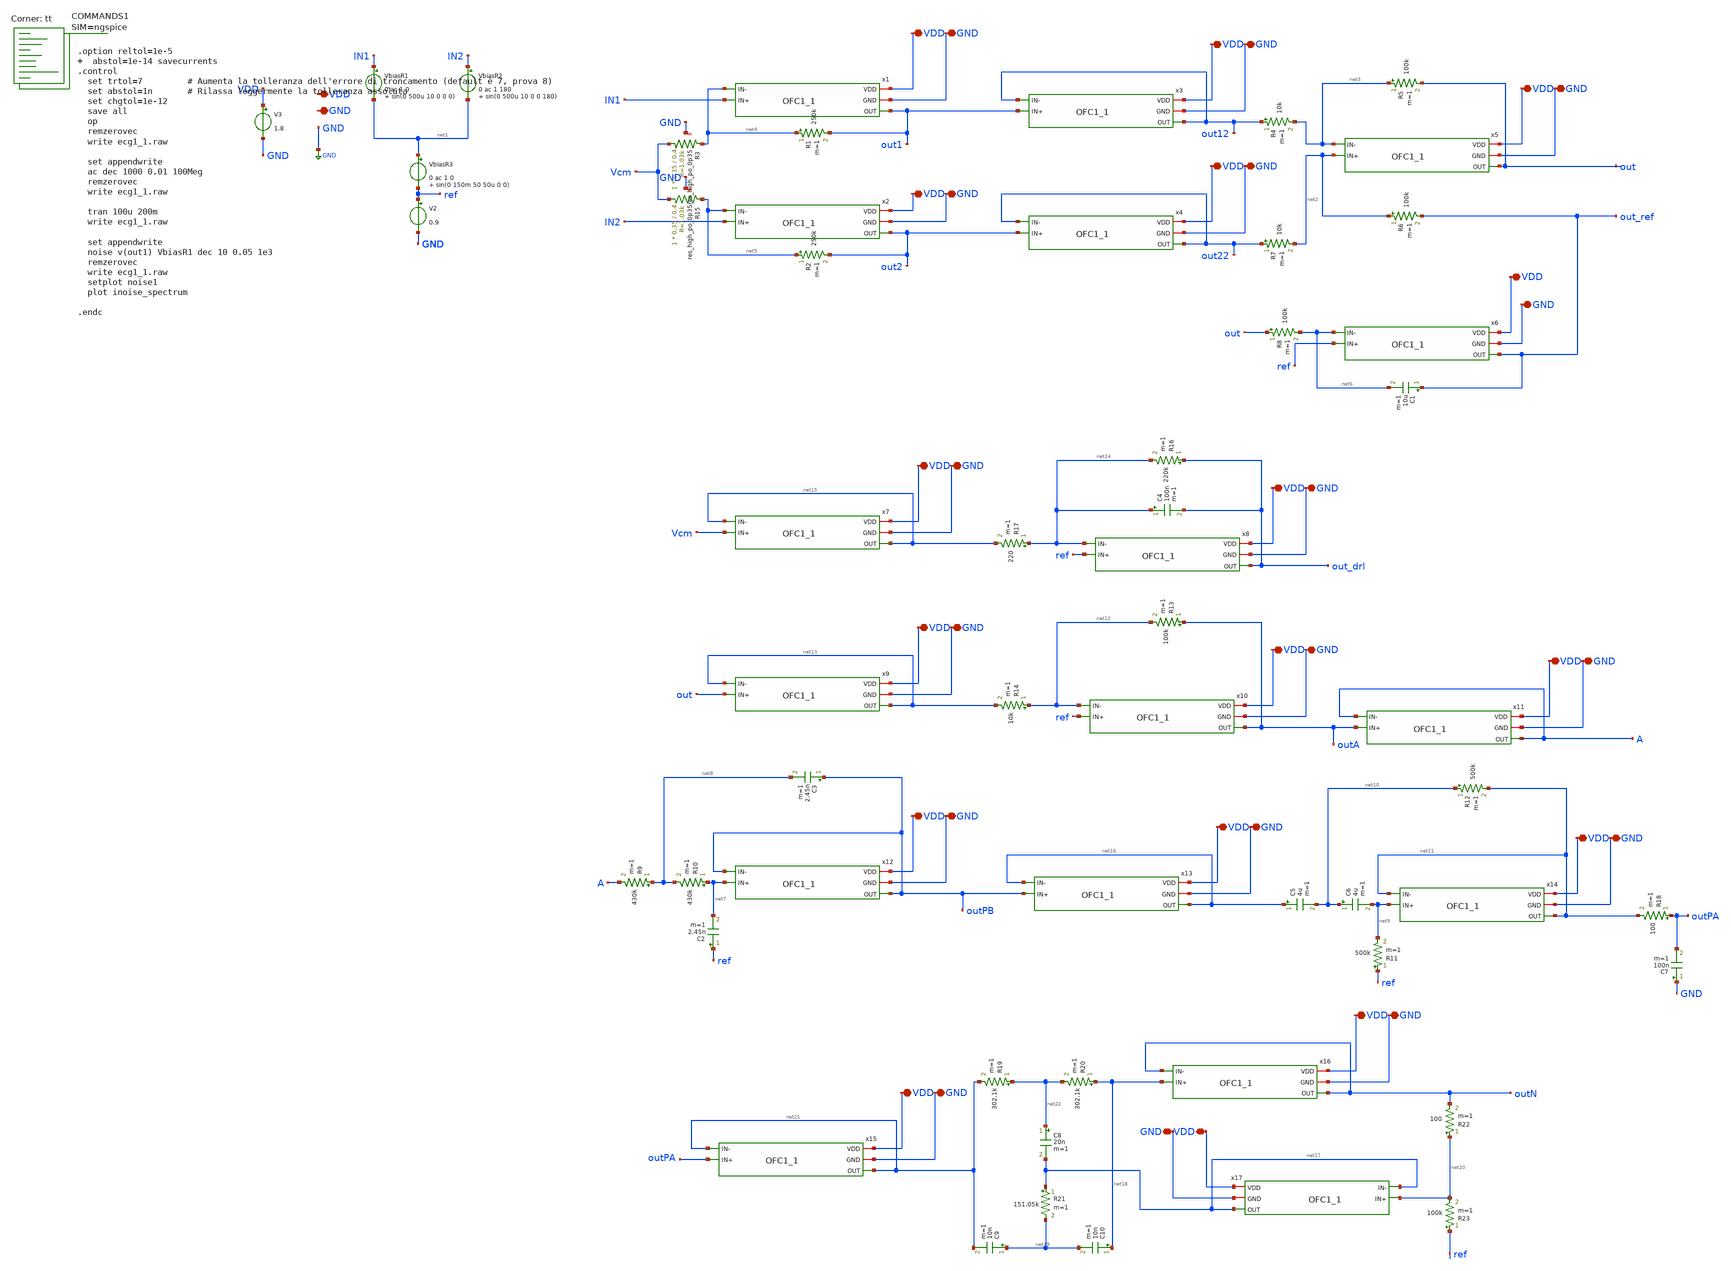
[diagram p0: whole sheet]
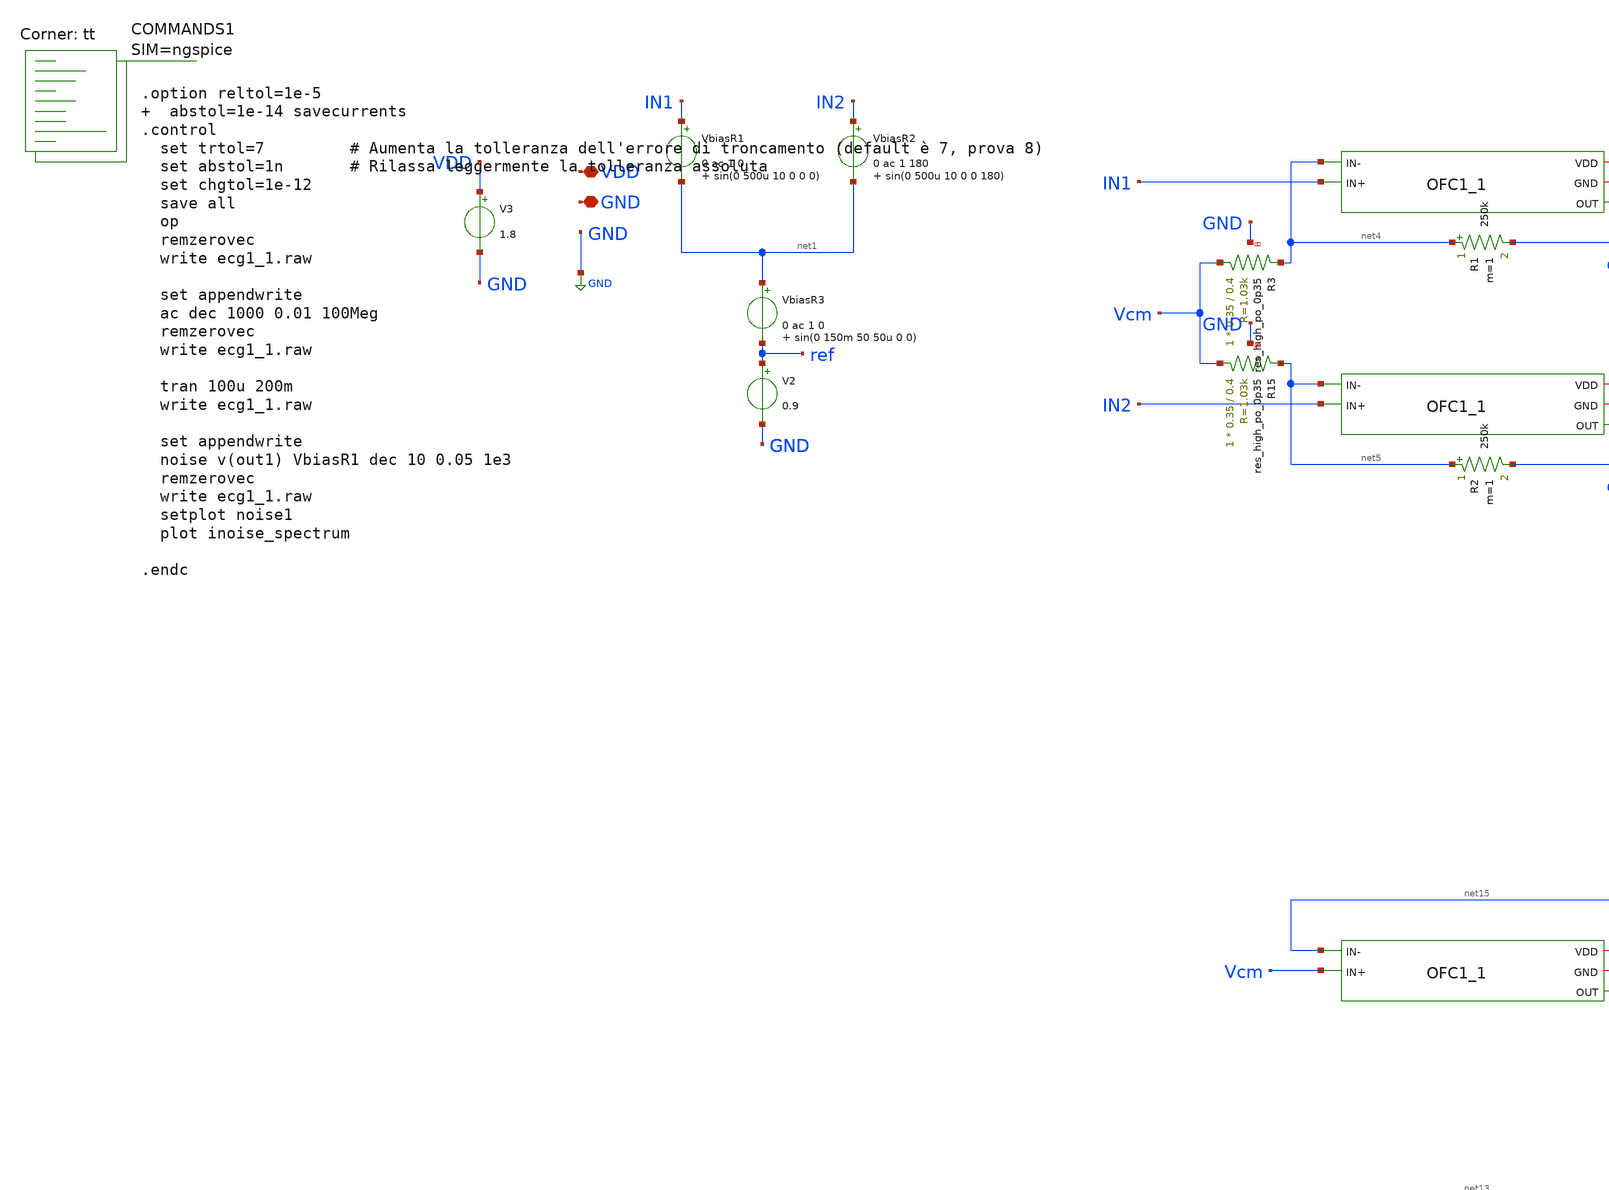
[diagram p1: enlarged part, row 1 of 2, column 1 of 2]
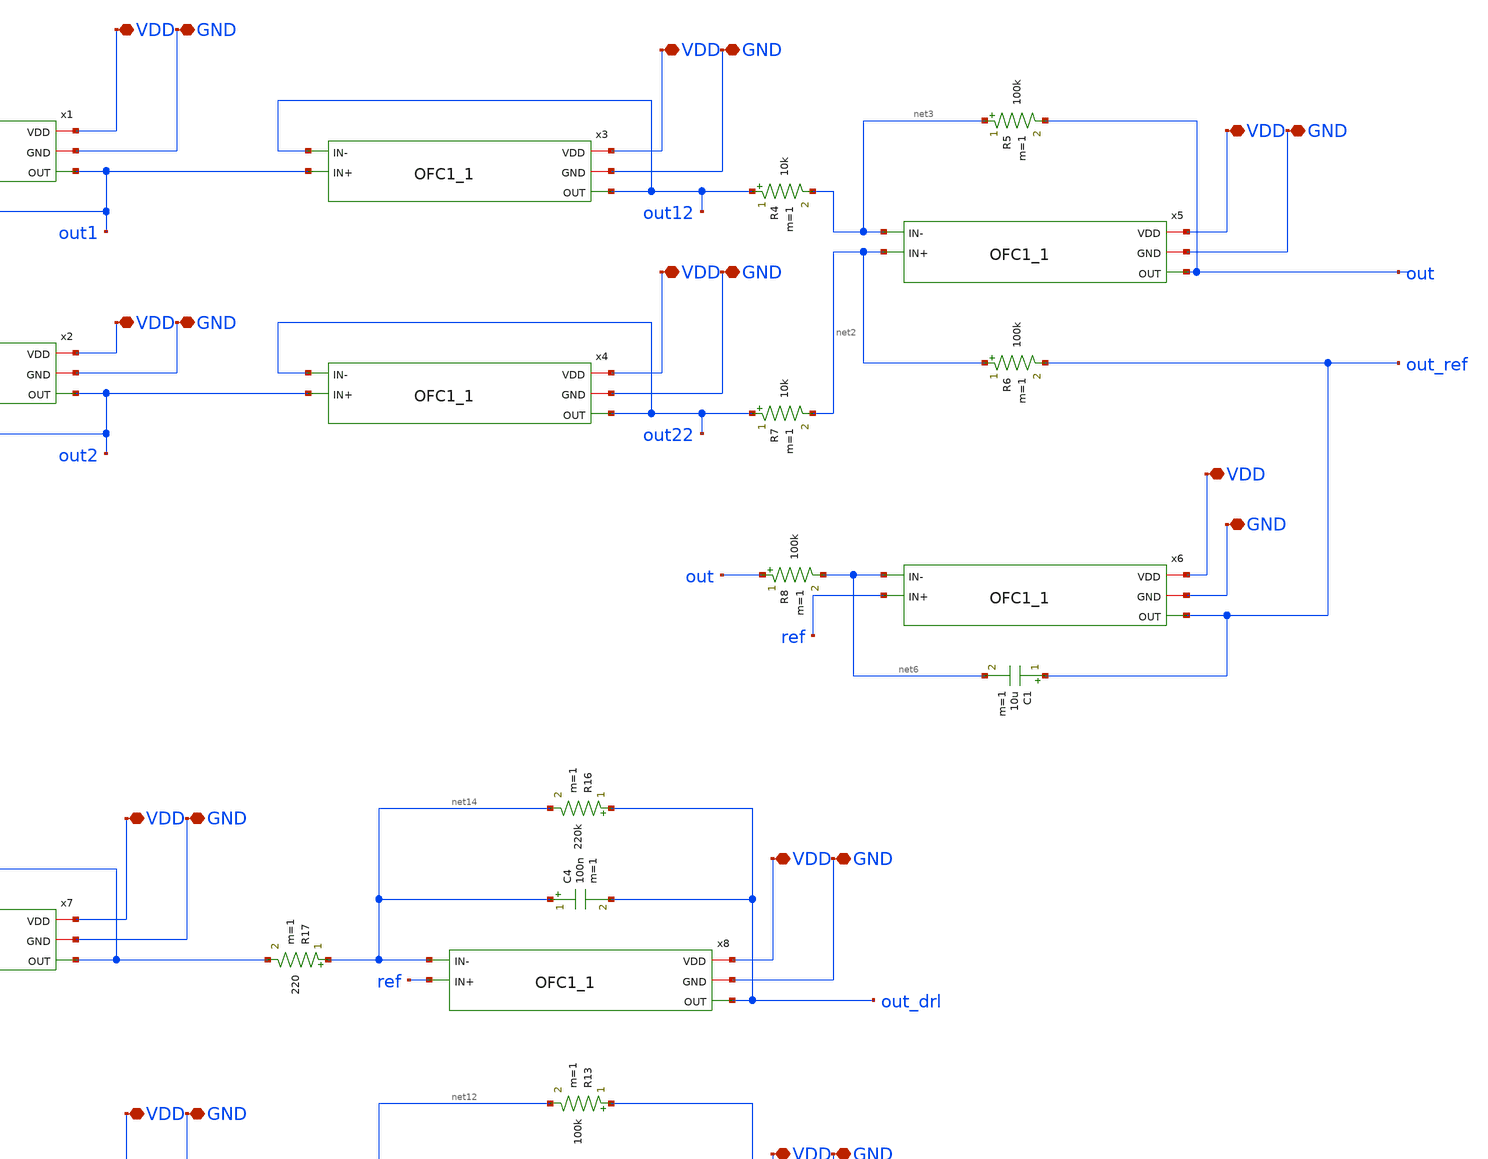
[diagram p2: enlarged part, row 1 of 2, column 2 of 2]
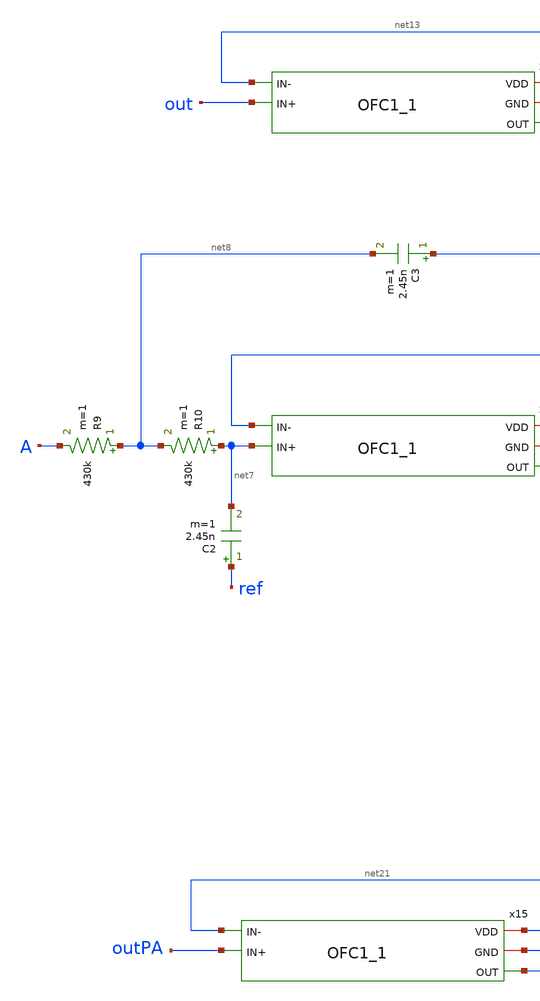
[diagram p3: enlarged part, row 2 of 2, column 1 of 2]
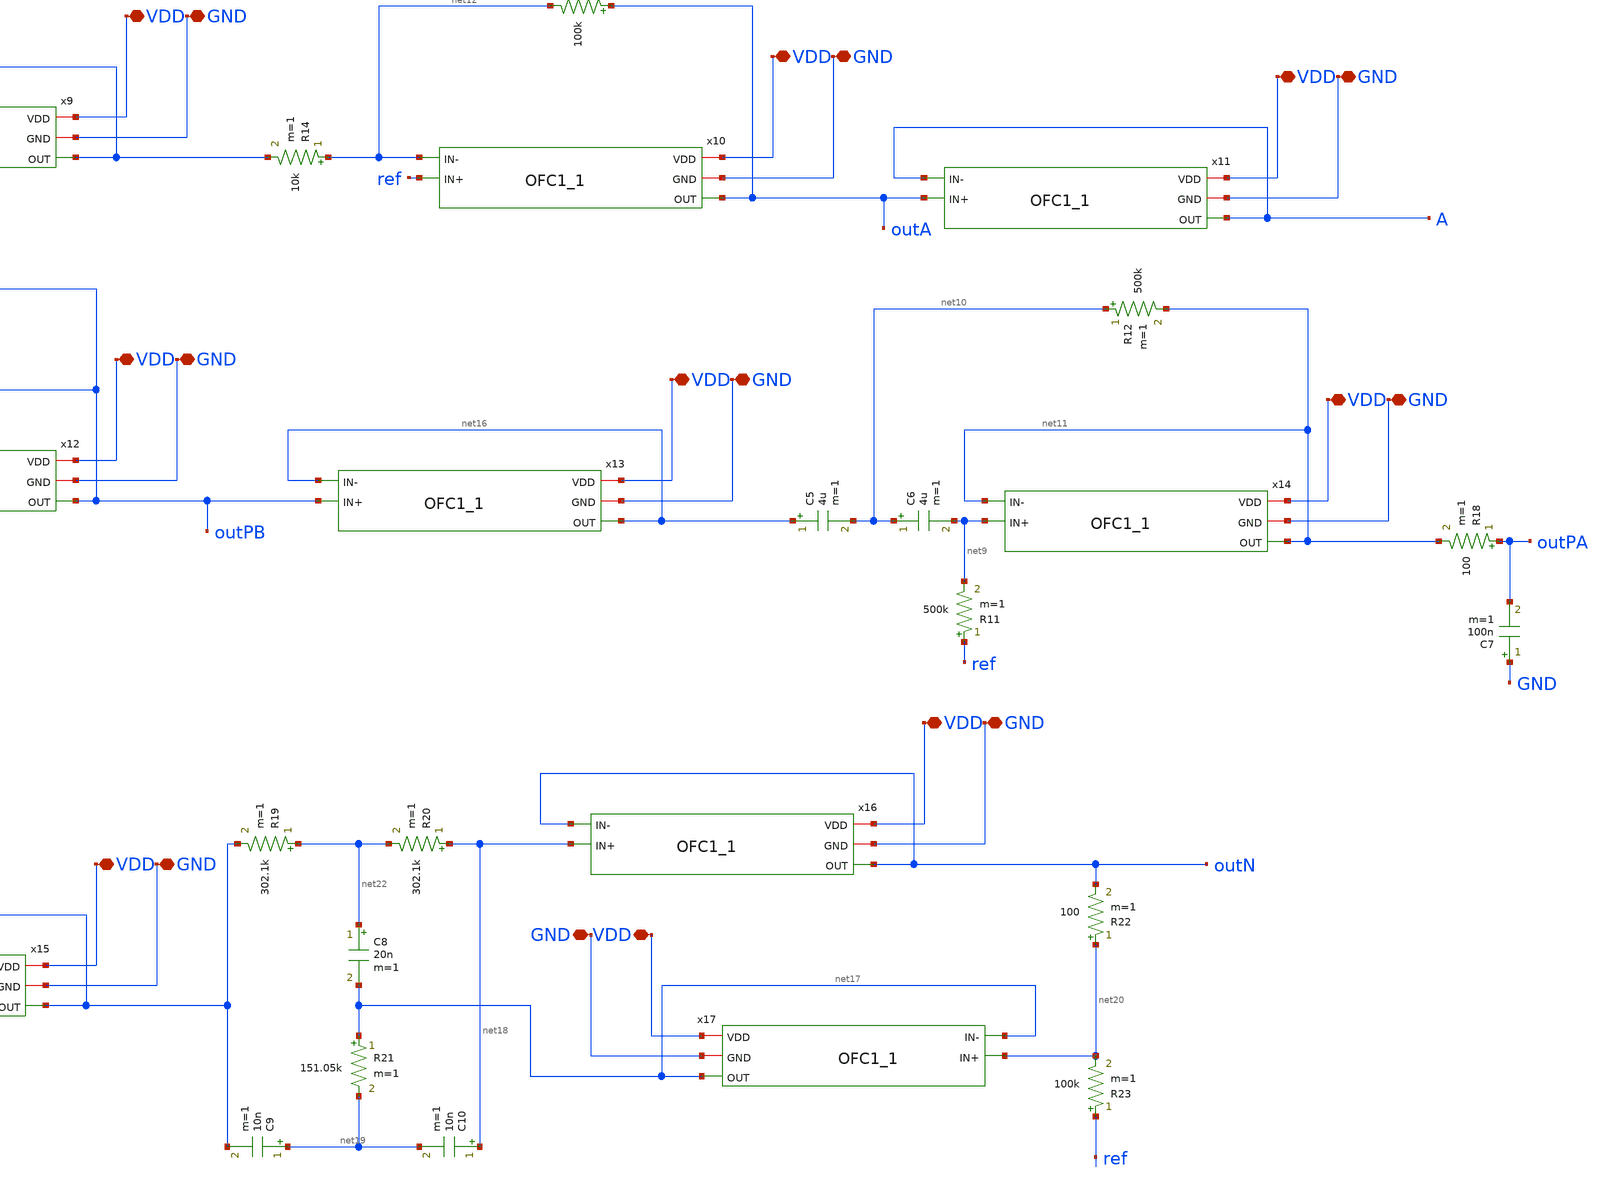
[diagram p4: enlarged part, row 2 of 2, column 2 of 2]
** sch_path: xschem/ecg1_1.sch
**.subckt ecg1_1 VDD GND VDD VDD GND GND VDD GND VDD GND VDD GND VDD GND VDD GND VDD GND VDD GND VDD
*+ GND VDD GND VDD GND VDD GND VDD GND VDD GND VDD GND VDD GND
*.iopin VDD
*.iopin GND
*.iopin VDD
*.iopin VDD
*.iopin GND
*.iopin GND
*.iopin VDD
*.iopin GND
*.iopin VDD
*.iopin GND
*.iopin VDD
*.iopin GND
*.iopin VDD
*.iopin GND
*.iopin VDD
*.iopin GND
*.iopin VDD
*.iopin GND
*.iopin VDD
*.iopin GND
*.iopin VDD
*.iopin GND
*.iopin VDD
*.iopin GND
*.iopin VDD
*.iopin GND
*.iopin VDD
*.iopin GND
*.iopin VDD
*.iopin GND
*.iopin VDD
*.iopin GND
*.iopin VDD
*.iopin GND
*.iopin VDD
*.iopin GND
V3 VDD GND 1.8
VbiasR1 IN1 net1 0 ac 1 0 sin(0 500u 10 0 0 0)
V2 ref GND 0.9
VbiasR2 IN2 net1 0 ac 1 180 sin(0 500u 10 0 0 180)
R1 net4 out1 250k m=1
R2 net5 out2 250k m=1
R6 net2 out_ref 100k m=1
R8 out net6 100k m=1
C1 out_ref net6 10u m=1
R5 net3 out 100k m=1
R4 out12 net3 10k m=1
R7 out22 net2 10k m=1
R9 net8 A 430k m=1
C2 ref net7 2.45n m=1
R10 net7 net8 430k m=1
C3 outPB net8 2.45n m=1
R11 ref net9 500k m=1
C5 net16 net10 4u m=1
C6 net10 net9 4u m=1
R13 outA net12 100k m=1
R14 net12 net13 10k m=1
R16 out_drl net14 220k m=1
R17 net14 net15 220 m=1
C4 net14 out_drl 100n m=1
C7 GND outPA 100n m=1
R18 outPA net11 100 m=1
R12 net10 net11 500k m=1
XR3 Vcm net4 GND sky130_fd_pr__res_high_po_0p35 L=0.4 mult=1 m=1
XR15 Vcm net5 GND sky130_fd_pr__res_high_po_0p35 L=0.4 mult=1 m=1
R19 net22 net21 302.1k m=1
R20 net18 net22 302.1k m=1
R21 net17 net19 151.05k m=1
C8 net22 net17 20n m=1
C9 net19 net21 10n m=1
C10 net18 net19 10n m=1
R22 net20 outN 100 m=1
R23 ref net20 100k m=1
x1 VDD GND out1 net4 IN1 OFC1_1
x2 VDD GND out2 net5 IN2 OFC1_1
x3 VDD GND out12 out12 out1 OFC1_1
x4 VDD GND out22 out22 out2 OFC1_1
x5 VDD GND out net3 net2 OFC1_1
x6 VDD GND out_ref net6 ref OFC1_1
x7 VDD GND net15 net15 Vcm OFC1_1
x8 VDD GND out_drl net14 ref OFC1_1
x9 VDD GND net13 net13 out OFC1_1
x10 VDD GND outA net12 ref OFC1_1
x11 VDD GND A A outA OFC1_1
x12 VDD GND outPB outPB net7 OFC1_1
x13 VDD GND net16 net16 outPB OFC1_1
x14 VDD GND net11 net11 net9 OFC1_1
x15 VDD GND net21 net21 outPA OFC1_1
x16 VDD GND outN outN net18 OFC1_1
x17 VDD GND net17 net17 net20 OFC1_1
VbiasR3 net1 ref 0 ac 1 0 sin(0 150m 50 50u 0 0)
**** begin user architecture code



.option reltol=1e-5   abstol=1e-14 savecurrents
.control
  set trtol=7         # Aumenta la tolleranza dell'errore di troncamento (default è 7, prova 8)
  set abstol=1n       # Rilassa leggermente la tolleranza assoluta
  set chgtol=1e-12
  save all
  op
  remzerovec
  write ecg1_1.raw

  set appendwrite
  ac dec 1000 0.01 100Meg
  remzerovec
  write ecg1_1.raw

  tran 100u 200m
  write ecg1_1.raw

  set appendwrite
  noise v(out1) VbiasR1 dec 10 0.05 1e3
  remzerovec
  write ecg1_1.raw
  setplot noise1
  plot inoise_spectrum

.endc



.lib $::SKYWATER_MODELS/sky130.lib.spice tt
**** end user architecture code
**.ends

* expanding   symbol:  OFC1_1.sym # of pins=5
** sym_path: xschem/OFC1_1.sym
** sch_path: xschem/OFC1_1.sch
.subckt OFC1_1 VDD GND OUT IN- IN+
*.iopin VDD
*.iopin GND
*.ipin IN+
*.ipin IN-
*.opin OUT
XR2 Vb VDD GND sky130_fd_pr__res_xhigh_po_0p35 L=5 mult=1 m=1
XR3 GND Vb GND sky130_fd_pr__res_xhigh_po_0p35 L=13.2 mult=1 m=1
XR1 Vc VDD GND sky130_fd_pr__res_xhigh_po_0p35 L=5 mult=1 m=1
XR4 GND Vc GND sky130_fd_pr__res_xhigh_po_0p35 L=3.07 mult=1 m=1
XR5 Vc1 VDD GND sky130_fd_pr__res_xhigh_po_0p35 L=5 mult=1 m=1
XR6 GND Vc1 GND sky130_fd_pr__res_xhigh_po_0p35 L=13.2 mult=1 m=1
XR7 Vc2 VDD GND sky130_fd_pr__res_xhigh_po_0p35 L=5 mult=1 m=1
XR8 GND Vc2 GND sky130_fd_pr__res_xhigh_po_0p35 L=1.4 mult=1 m=1
XM11 S Vb VDD VDD sky130_fd_pr__pfet_01v8_lvt L=1 W=45 nf=3 ad='int((nf+1)/2) * W/nf * 0.29' as='int((nf+2)/2)
+ * W/nf * 0.29' pd='2*int((nf+1)/2) * (W/nf + 0.29)' ps='2*int((nf+2)/2) * (W/nf + 0.29)' nrd='0.29 /
+ W' nrs='0.29 / W' sa=0 sb=0 sd=0 mult=10 m=10
XM1 D1 IN+ S S sky130_fd_pr__pfet_01v8_lvt L=10 W=50 nf=2 ad='int((nf+1)/2) * W/nf * 0.29' as='int((nf+2)/2)
+ * W/nf * 0.29' pd='2*int((nf+1)/2) * (W/nf + 0.29)' ps='2*int((nf+2)/2) * (W/nf + 0.29)' nrd='0.29 /
+ W' nrs='0.29 / W' sa=0 sb=0 sd=0 mult=2 m=2
XM2 D2 IN- S S sky130_fd_pr__pfet_01v8_lvt L=10 W=50 nf=2 ad='int((nf+1)/2) * W/nf * 0.29' as='int((nf+2)/2)
+ * W/nf * 0.29' pd='2*int((nf+1)/2) * (W/nf + 0.29)' ps='2*int((nf+2)/2) * (W/nf + 0.29)' nrd='0.29 /
+ W' nrs='0.29 / W' sa=0 sb=0 sd=0 mult=2 m=2
XM3 OUT Vc1 D2 GND sky130_fd_pr__nfet_01v8_lvt L=1 W=4 nf=1 ad='int((nf+1)/2) * W/nf * 0.29' as='int((nf+2)/2)
+ * W/nf * 0.29' pd='2*int((nf+1)/2) * (W/nf + 0.29)' ps='2*int((nf+2)/2) * (W/nf + 0.29)' nrd='0.29 /
+ W' nrs='0.29 / W' sa=0 sb=0 sd=0 mult=1 m=1
XM4 D2 Vc GND GND sky130_fd_pr__nfet_01v8_lvt L=1 W=8 nf=1 ad='int((nf+1)/2) * W/nf * 0.29' as='int((nf+2)/2)
+ * W/nf * 0.29' pd='2*int((nf+1)/2) * (W/nf + 0.29)' ps='2*int((nf+2)/2) * (W/nf + 0.29)' nrd='0.29 /
+ W' nrs='0.29 / W' sa=0 sb=0 sd=0 mult=1 m=1
XM5 D1 Vc GND GND sky130_fd_pr__nfet_01v8_lvt L=1 W=8 nf=1 ad='int((nf+1)/2) * W/nf * 0.29' as='int((nf+2)/2)
+ * W/nf * 0.29' pd='2*int((nf+1)/2) * (W/nf + 0.29)' ps='2*int((nf+2)/2) * (W/nf + 0.29)' nrd='0.29 /
+ W' nrs='0.29 / W' sa=0 sb=0 sd=0 mult=1 m=1
XM6 G Vc1 D1 GND sky130_fd_pr__nfet_01v8_lvt L=1 W=4 nf=1 ad='int((nf+1)/2) * W/nf * 0.29' as='int((nf+2)/2)
+ * W/nf * 0.29' pd='2*int((nf+1)/2) * (W/nf + 0.29)' ps='2*int((nf+2)/2) * (W/nf + 0.29)' nrd='0.29 /
+ W' nrs='0.29 / W' sa=0 sb=0 sd=0 mult=1 m=1
XM7 G Vc2 D9 VDD sky130_fd_pr__pfet_01v8_lvt L=1.2 W=8 nf=1 ad='int((nf+1)/2) * W/nf * 0.29' as='int((nf+2)/2)
+ * W/nf * 0.29' pd='2*int((nf+1)/2) * (W/nf + 0.29)' ps='2*int((nf+2)/2) * (W/nf + 0.29)' nrd='0.29 /
+ W' nrs='0.29 / W' sa=0 sb=0 sd=0 mult=1 m=1
XM9 D9 G VDD VDD sky130_fd_pr__pfet_01v8_lvt L=1.2 W=5.7 nf=1 ad='int((nf+1)/2) * W/nf * 0.29' as='int((nf+2)/2)
+ * W/nf * 0.29' pd='2*int((nf+1)/2) * (W/nf + 0.29)' ps='2*int((nf+2)/2) * (W/nf + 0.29)' nrd='0.29 /
+ W' nrs='0.29 / W' sa=0 sb=0 sd=0 mult=1 m=1
XM8 D10 G VDD VDD sky130_fd_pr__pfet_01v8_lvt L=1.2 W=5.7 nf=1 ad='int((nf+1)/2) * W/nf * 0.29' as='int((nf+2)/2)
+ * W/nf * 0.29' pd='2*int((nf+1)/2) * (W/nf + 0.29)' ps='2*int((nf+2)/2) * (W/nf + 0.29)' nrd='0.29 /
+ W' nrs='0.29 / W' sa=0 sb=0 sd=0 mult=1 m=1
XM10 OUT Vc2 D10 VDD sky130_fd_pr__pfet_01v8_lvt L=1.2 W=8 nf=1 ad='int((nf+1)/2) * W/nf * 0.29' as='int((nf+2)/2)
+ * W/nf * 0.29' pd='2*int((nf+1)/2) * (W/nf + 0.29)' ps='2*int((nf+2)/2) * (W/nf + 0.29)' nrd='0.29 /
+ W' nrs='0.29 / W' sa=0 sb=0 sd=0 mult=1 m=1
.ends

.GLOBAL GND
.end
